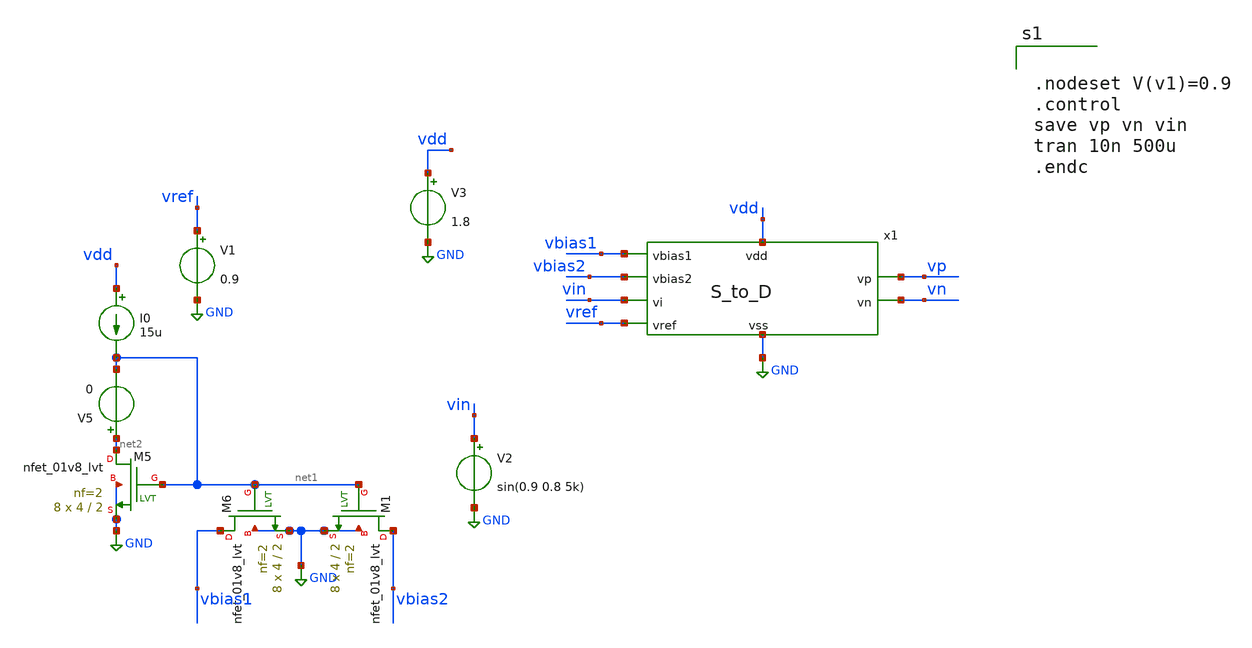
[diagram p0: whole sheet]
** sch_path: xschem/src/S_to_D/S_to_D_tb.sch
**.subckt S_to_D_tb
V3 vdd GND 1.8
V2 vin GND sin(0.9 0.8 5k)
V1 vref GND 0.9
I0 vdd net1 15u
XM5 net2 net1 GND GND sky130_fd_pr__nfet_01v8_lvt L=2 W=4 nf=2 ad='int((nf+1)/2) * W/nf * 0.29' as='int((nf+2)/2) * W/nf * 0.29'
+ pd='2*int((nf+1)/2) * (W/nf + 0.29)' ps='2*int((nf+2)/2) * (W/nf + 0.29)' nrd='0.29 / W' nrs='0.29 / W'
+ sa=0 sb=0 sd=0 mult=8 m=8
XM6 vbias1 net1 GND GND sky130_fd_pr__nfet_01v8_lvt L=2 W=4 nf=2 ad='int((nf+1)/2) * W/nf * 0.29' as='int((nf+2)/2) * W/nf * 0.29'
+ pd='2*int((nf+1)/2) * (W/nf + 0.29)' ps='2*int((nf+2)/2) * (W/nf + 0.29)' nrd='0.29 / W' nrs='0.29 / W'
+ sa=0 sb=0 sd=0 mult=8 m=8
V5 net2 net1 0
XM1 vbias2 net1 GND GND sky130_fd_pr__nfet_01v8_lvt L=2 W=4 nf=2 ad='int((nf+1)/2) * W/nf * 0.29' as='int((nf+2)/2) * W/nf * 0.29'
+ pd='2*int((nf+1)/2) * (W/nf + 0.29)' ps='2*int((nf+2)/2) * (W/nf + 0.29)' nrd='0.29 / W' nrs='0.29 / W'
+ sa=0 sb=0 sd=0 mult=8 m=8
x1 vdd vbias1 vbias2 vin vref GND vn vp S_to_D
**** begin user architecture code


.nodeset V(v1)=0.9
.control
save vp vn vin
tran 10n 500u
.endc



.include /home/eda/pdk/skywater-pdk/libraries/sky130_fd_pr_ngspice/latest/models/corners/ss.spice
.include /home/eda/magic/class_d_audio_amplifier/S_to_D/S_to_D_post.spice

.include /home/eda/magic/class_d_audio_amplifier/S_to_D/S_to_D_revised_post.spice

* Resistor$::SKYWATER_MODELS/Capacitor
.include $::SKYWATER_MODELS/models/r+c/res_typical__cap_typical.spice
.include $::SKYWATER_MODELS/models/r+c/res_typical__cap_typical__lin.spice
* Special cells
.include $::SKYWATER_MODELS/models/corners/tt/specialized_cells.spice


**** end user architecture code
**.ends

* expanding   symbol:  src/S_to_D/S_to_D.sym # of pins=8
** sym_path: xschem/src/S_to_D/S_to_D.sym
** sch_path: xschem/src/S_to_D/S_to_D.sch
.subckt S_to_D vdd vbias1 vbias2 vi vref vss vn vp
*.iopin vdd
*.iopin vss
*.ipin vi
*.opin vp
*.opin vn
*.ipin vref
*.ipin vbias1
*.ipin vbias2
x1 vdd vref v1 vbias2 vss vn OTA
XR2 vn v1 vss sky130_fd_pr__res_xhigh_po L=10 mult=1 m=1
x2 vdd vi vp vbias1 vss vp OTA
XR1 v1 vi vss sky130_fd_pr__res_xhigh_po L=10 mult=1 m=1
.ends


* expanding   symbol:  src/OTA/OTA.sym # of pins=6
** sym_path: xschem/src/OTA/OTA.sym
** sch_path: xschem/src/OTA/OTA.sch
.subckt OTA vdd vp vn vbias vss vout
*.ipin vp
*.ipin vn
*.ipin vbias
*.iopin vss
*.iopin vdd
*.opin vout
XM1 v1 vp vc vc sky130_fd_pr__pfet_01v8_lvt L=1 W=4 nf=1 ad='int((nf+1)/2) * W/nf * 0.29' as='int((nf+2)/2) * W/nf * 0.29'
+ pd='2*int((nf+1)/2) * (W/nf + 0.29)' ps='2*int((nf+2)/2) * (W/nf + 0.29)' nrd='0.29 / W' nrs='0.29 / W'
+ sa=0 sb=0 sd=0 mult=16 m=16
XM2 vf vn vc vc sky130_fd_pr__pfet_01v8_lvt L=1 W=4 nf=1 ad='int((nf+1)/2) * W/nf * 0.29' as='int((nf+2)/2) * W/nf * 0.29'
+ pd='2*int((nf+1)/2) * (W/nf + 0.29)' ps='2*int((nf+2)/2) * (W/nf + 0.29)' nrd='0.29 / W' nrs='0.29 / W'
+ sa=0 sb=0 sd=0 mult=16 m=16
XM3 vc vbias vdd vdd sky130_fd_pr__pfet_01v8_lvt L=1 W=2 nf=2 ad='int((nf+1)/2) * W/nf * 0.29' as='int((nf+2)/2) * W/nf * 0.29'
+ pd='2*int((nf+1)/2) * (W/nf + 0.29)' ps='2*int((nf+2)/2) * (W/nf + 0.29)' nrd='0.29 / W' nrs='0.29 / W'
+ sa=0 sb=0 sd=0 mult=24 m=24
XM4 v1 vf vss vss sky130_fd_pr__nfet_01v8_lvt L=1 W=1 nf=1 ad='int((nf+1)/2) * W/nf * 0.29' as='int((nf+2)/2) * W/nf * 0.29'
+ pd='2*int((nf+1)/2) * (W/nf + 0.29)' ps='2*int((nf+2)/2) * (W/nf + 0.29)' nrd='0.29 / W' nrs='0.29 / W'
+ sa=0 sb=0 sd=0 mult=16 m=16
XM5 vf vf vss vss sky130_fd_pr__nfet_01v8_lvt L=1 W=1 nf=1 ad='int((nf+1)/2) * W/nf * 0.29' as='int((nf+2)/2) * W/nf * 0.29'
+ pd='2*int((nf+1)/2) * (W/nf + 0.29)' ps='2*int((nf+2)/2) * (W/nf + 0.29)' nrd='0.29 / W' nrs='0.29 / W'
+ sa=0 sb=0 sd=0 mult=16 m=16
XM6 vbias vbias vdd vdd sky130_fd_pr__pfet_01v8_lvt L=1 W=2 nf=2 ad='int((nf+1)/2) * W/nf * 0.29' as='int((nf+2)/2) * W/nf * 0.29'
+ pd='2*int((nf+1)/2) * (W/nf + 0.29)' ps='2*int((nf+2)/2) * (W/nf + 0.29)' nrd='0.29 / W' nrs='0.29 / W'
+ sa=0 sb=0 sd=0 mult=24 m=24
XM7 vout vbias vdd vdd sky130_fd_pr__pfet_01v8_lvt L=1 W=2 nf=2 ad='int((nf+1)/2) * W/nf * 0.29' as='int((nf+2)/2) * W/nf * 0.29'
+ pd='2*int((nf+1)/2) * (W/nf + 0.29)' ps='2*int((nf+2)/2) * (W/nf + 0.29)' nrd='0.29 / W' nrs='0.29 / W'
+ sa=0 sb=0 sd=0 mult=48 m=48
XM8 vout v1 vss vss sky130_fd_pr__nfet_01v8_lvt L=1 W=1 nf=1 ad='int((nf+1)/2) * W/nf * 0.29' as='int((nf+2)/2) * W/nf * 0.29'
+ pd='2*int((nf+1)/2) * (W/nf + 0.29)' ps='2*int((nf+2)/2) * (W/nf + 0.29)' nrd='0.29 / W' nrs='0.29 / W'
+ sa=0 sb=0 sd=0 mult=64 m=64
XR1 v1 net1 vss sky130_fd_pr__res_xhigh_po W=0.35 L=0.5 mult=1 m=1
XC2 net1 vout sky130_fd_pr__cap_mim_m3_1 W=14 L=14 MF=1 m=1
.ends

.GLOBAL GND
.end
